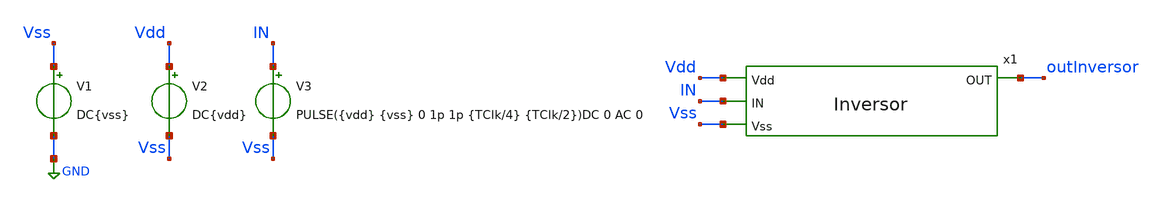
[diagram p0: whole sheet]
** sch_path: icdesign/sch/Inversor/Tb_Inversor.sch
**.subckt Tb_Inversor
V1 Vss GND DC{vss}
V2 Vdd Vss DC{vdd}
V3 IN Vss PULSE({vdd} {vss} 0 1p 1p {TClk/4} {TClk/2})DC 0 AC 0
x1 Vdd IN outInversor Vss Inversor
**** begin user architecture code





* Circuit Parameters
.param vdd  = 1.8
.param vss  = 0.0
.param Tclk = 10n
.options TEMP = 65.0


* Include Models
.lib ~/skywater/skywater-pdk/libraries/sky130_fd_pr_ngspice/latest/models/corners/sky130.lib TT


* OP Parameters & Singals to save
.save all


*Simulations
.control
  tran 0.01u 100n
  setplot tran1
  plot v(IN) v(outInversor)+2
.endc
.end


**** end user architecture code
**.ends

* expanding   symbol:  Inversor/Inversor.sym # of pins=4
** sym_path: icdesign/sch/Inversor/Inversor.sym
** sch_path: icdesign/sch/Inversor/Inversor.sch
.subckt Inversor Vdd IN OUT Vss
*.ipin IN
*.ipin Vdd
*.ipin Vss
*.opin OUT
XM1 OUT IN Vss Vss sky130_fd_pr__nfet_01v8 L=0.15 W=0.75 nf=1 ad='int((nf+1)/2) * W/nf * 0.29' as='int((nf+2)/2) * W/nf * 0.29'
+ pd='2*int((nf+1)/2) * (W/nf + 0.29)' ps='2*int((nf+2)/2) * (W/nf + 0.29)' nrd='0.29 / W' nrs='0.29 / W'
+ sa=0 sb=0 sd=0 mult=1 m=1
XM2 OUT IN Vdd Vdd sky130_fd_pr__pfet_01v8 L=0.15 W=0.75 nf=1 ad='int((nf+1)/2) * W/nf * 0.29' as='int((nf+2)/2) * W/nf * 0.29'
+ pd='2*int((nf+1)/2) * (W/nf + 0.29)' ps='2*int((nf+2)/2) * (W/nf + 0.29)' nrd='0.29 / W' nrs='0.29 / W'
+ sa=0 sb=0 sd=0 mult=2 m=2
.ends

.GLOBAL GND
.end
